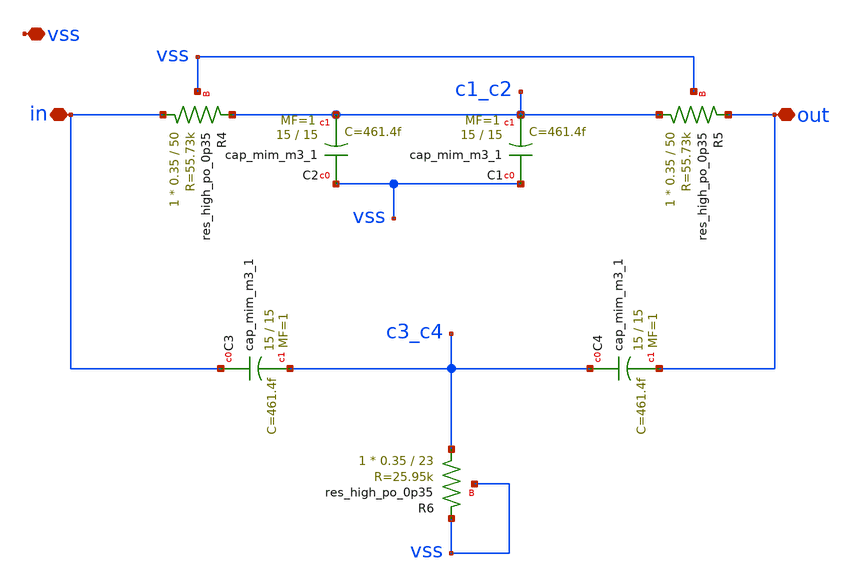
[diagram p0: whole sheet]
** sch_path: xschem/twin_tee.sch
**.subckt twin_tee vss in out
*.iopin vss
*.iopin in
*.iopin out
XR5 c1_c2 out vss sky130_fd_pr__res_high_po_0p35 L=50 mult=1 m=1
XC1 vss c1_c2 sky130_fd_pr__cap_mim_m3_1 W=15 L=15 MF=1 m=1
XC2 vss c1_c2 sky130_fd_pr__cap_mim_m3_1 W=15 L=15 MF=1 m=1
XR4 in c1_c2 vss sky130_fd_pr__res_high_po_0p35 L=50 mult=1 m=1
XC3 in c3_c4 sky130_fd_pr__cap_mim_m3_1 W=15 L=15 MF=1 m=1
XC4 c3_c4 out sky130_fd_pr__cap_mim_m3_1 W=15 L=15 MF=1 m=1
XR6 c3_c4 vss vss sky130_fd_pr__res_high_po_0p35 L=23 mult=1 m=1
**.ends
.end
